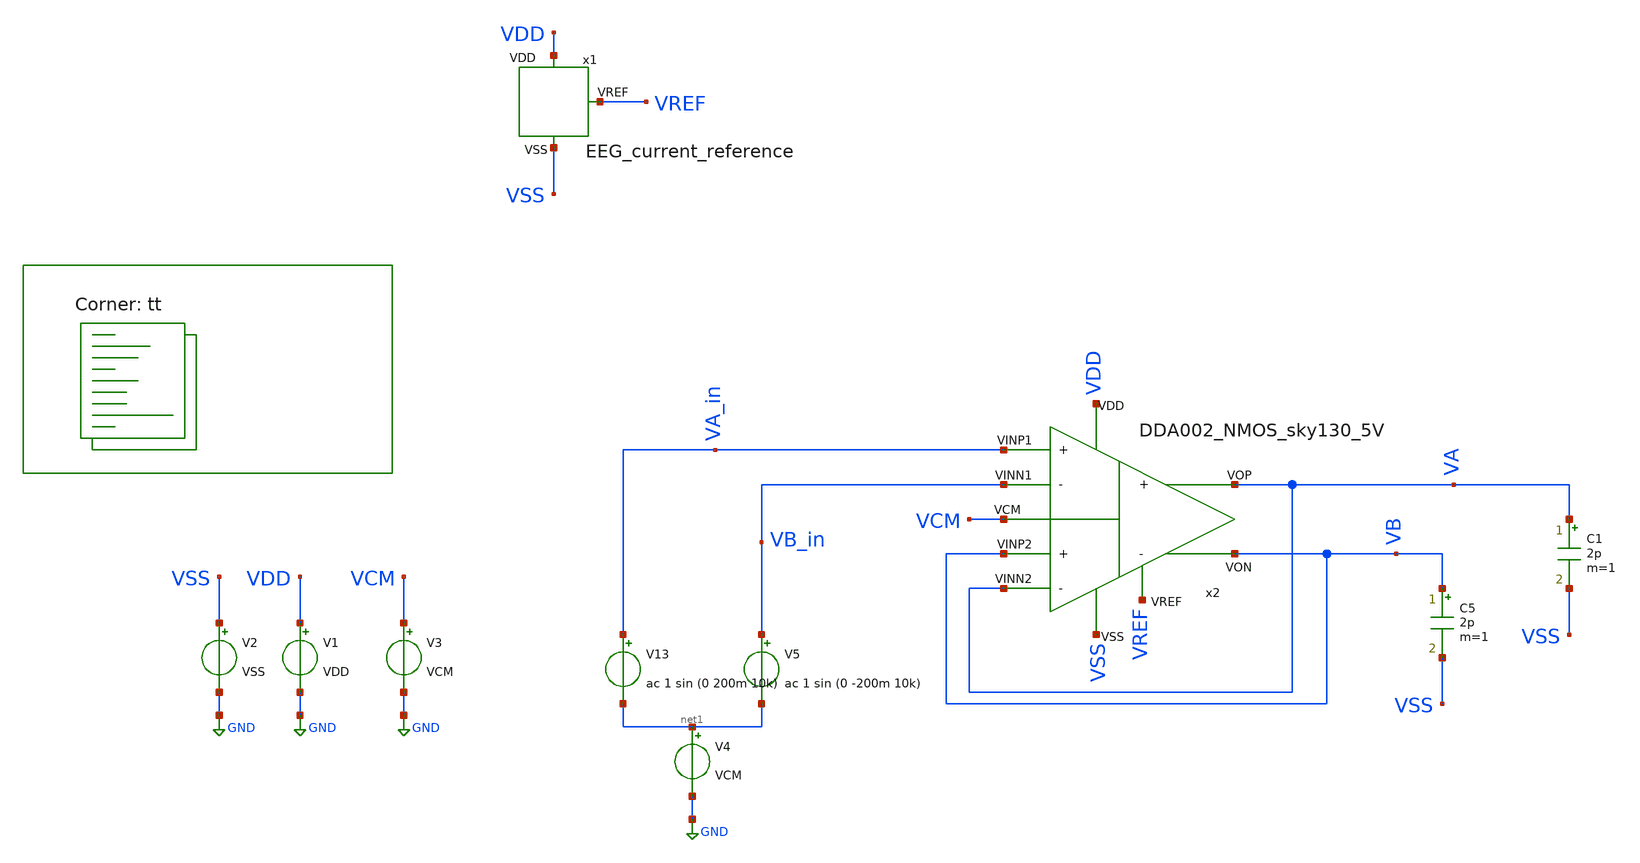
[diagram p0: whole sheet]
** sch_path: Learning/complex_projects/A_Two-Stage_Time_Division_Multiplexing_AFE_with_Input_Impedance_Boosting_DDA_for_EEG_Signal_Acquisition/sky130A_5V/input_buffer_chopper/buffer_stage.sch
**.subckt buffer_stage
V1 VDD GND VDD
V2 VSS GND VSS
x1 VDD VSS VREF EEG_current_reference
x2 VDD VSS VREF VB_in VA VA_in VB VCM VA VB DDA002_NMOS_sky130_5V
V3 VCM GND VCM
V4 net1 GND VCM
C5 VB VSS 2p m=1
C1 VA VSS 2p m=1
V13 VA_in net1 ac 1 sin (0 200m 10k)
V5 VB_in net1 ac 1 sin (0 -200m 10k)
**** begin user architecture code
.lib $::SKYWATER_MODELS/sky130.lib.spice tt

.Temp 27
.param VDD = 5
.param VSS = 0
.param CL = 3p
.param V_OFF = -400u
.param VCM = 2.5


.control

	save all
        tran 10ns 500u
	plot v(VB) v(VB_in)
	plot v(VA_in) v(VA)

.endc




**** end user architecture code
**.ends
.GLOBAL GND
.end
